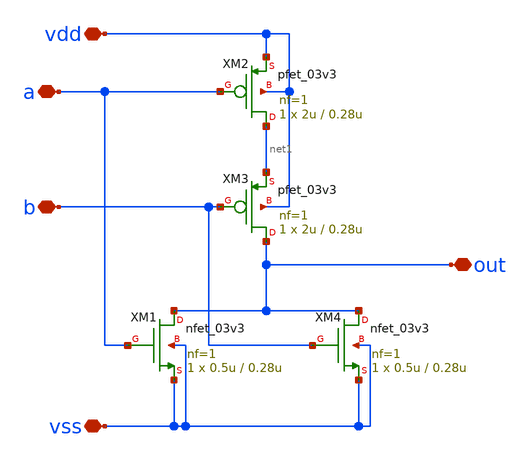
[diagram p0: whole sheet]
** sch_path: designs/libs/qw_core_analog_pkedit/NOR.sch
**.subckt NOR vdd vss a b out
*.iopin vdd
*.iopin vss
*.iopin a
*.iopin b
*.iopin out
XM1 out a vss vss nfet_03v3 L=0.28u W=0.5u nf=1 ad='int((nf+1)/2) * W/nf * 0.18u' as='int((nf+2)/2) * W/nf * 0.18u'
+ pd='2*int((nf+1)/2) * (W/nf + 0.18u)' ps='2*int((nf+2)/2) * (W/nf + 0.18u)' nrd='0.18u / W' nrs='0.18u / W'
+ sa=0 sb=0 sd=0 m=1
XM2 net1 a vdd vdd pfet_03v3 L=0.28u W=2u nf=1 ad='int((nf+1)/2) * W/nf * 0.18u' as='int((nf+2)/2) * W/nf * 0.18u'
+ pd='2*int((nf+1)/2) * (W/nf + 0.18u)' ps='2*int((nf+2)/2) * (W/nf + 0.18u)' nrd='0.18u / W' nrs='0.18u / W'
+ sa=0 sb=0 sd=0 m=1
XM3 out b net1 vdd pfet_03v3 L=0.28u W=2u nf=1 ad='int((nf+1)/2) * W/nf * 0.18u' as='int((nf+2)/2) * W/nf * 0.18u'
+ pd='2*int((nf+1)/2) * (W/nf + 0.18u)' ps='2*int((nf+2)/2) * (W/nf + 0.18u)' nrd='0.18u / W' nrs='0.18u / W'
+ sa=0 sb=0 sd=0 m=1
XM4 out b vss vss nfet_03v3 L=0.28u W=0.5u nf=1 ad='int((nf+1)/2) * W/nf * 0.18u' as='int((nf+2)/2) * W/nf * 0.18u'
+ pd='2*int((nf+1)/2) * (W/nf + 0.18u)' ps='2*int((nf+2)/2) * (W/nf + 0.18u)' nrd='0.18u / W' nrs='0.18u / W'
+ sa=0 sb=0 sd=0 m=1
**.ends
.end
